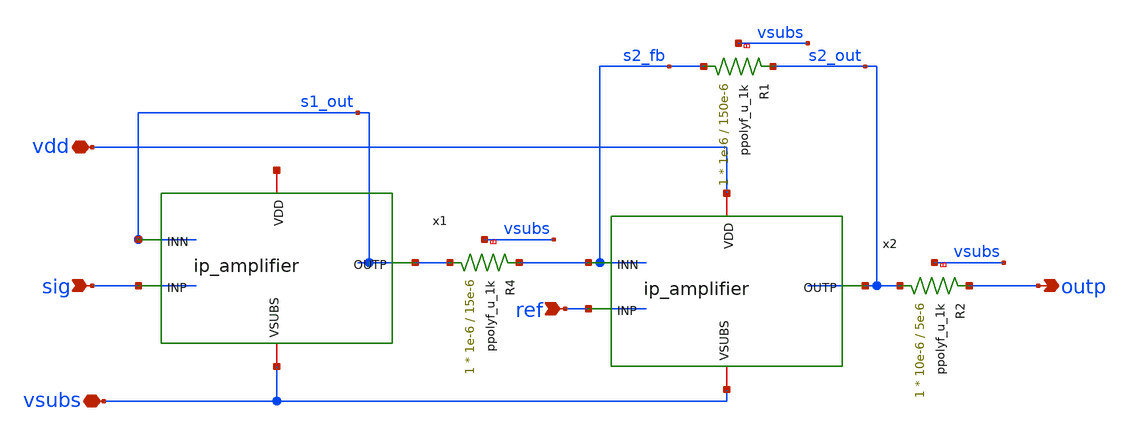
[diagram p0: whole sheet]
** sch_path: xschem/ip_sigproc.sch
**.subckt ip_sigproc sig ref vdd vsubs outp
*.ipin sig
*.ipin ref
*.iopin vdd
*.iopin vsubs
*.opin outp
x1 net1 s1_out sig s1_out vsubs ip_amplifier
x2 vdd s2_out ref s2_fb vsubs ip_amplifier
XR4 s1_out s2_fb vsubs ppolyf_u_1k r_width=1e-6 r_length=15e-6 m=1
XR1 s2_fb s2_out vsubs ppolyf_u_1k r_width=1e-6 r_length=150e-6 m=1
XR2 s2_out outp vsubs ppolyf_u_1k r_width=10e-6 r_length=5e-6 m=1
**.ends

* expanding   symbol:  ip_amplifier.sym # of pins=5
** sym_path: xschem/ip_amplifier.sym
** sch_path: xschem/ip_amplifier.sch
.subckt ip_amplifier VDD OUTP INP INN VSUBS
*.iopin VDD
*.iopin VSUBS
*.ipin INP
*.ipin INN
*.opin OUTP
XM1 net10 INP net8 VDD pfet_06v0 L=0.7u W=11.0u nf=1 ad='int((nf+1)/2) * W/nf * 0.18u' as='int((nf+2)/2) * W/nf * 0.18u'
+ pd='2*int((nf+1)/2) * (W/nf + 0.18u)' ps='2*int((nf+2)/2) * (W/nf + 0.18u)' nrd='0.18u / W' nrs='0.18u / W'
+ sa=0 sb=0 sd=0 m=2 par=2
XM2 net9 INN net8 VDD pfet_06v0 L=0.7u W=11.0u nf=1 ad='int((nf+1)/2) * W/nf * 0.18u' as='int((nf+2)/2) * W/nf * 0.18u'
+ pd='2*int((nf+1)/2) * (W/nf + 0.18u)' ps='2*int((nf+2)/2) * (W/nf + 0.18u)' nrd='0.18u / W' nrs='0.18u / W'
+ sa=0 sb=0 sd=0 m=2 par=2
XM5 net10 net1 VSUBS vsubs nfet_06v0 L=2u W=5u nf=1 ad='int((nf+1)/2) * W/nf * 0.18u' as='int((nf+2)/2) * W/nf * 0.18u'
+ pd='2*int((nf+1)/2) * (W/nf + 0.18u)' ps='2*int((nf+2)/2) * (W/nf + 0.18u)' nrd='0.18u / W' nrs='0.18u / W'
+ sa=0 sb=0 sd=0 m=1 par=1
XM6 net9 net1 VSUBS vsubs nfet_06v0 L=2u W=5u nf=1 ad='int((nf+1)/2) * W/nf * 0.18u' as='int((nf+2)/2) * W/nf * 0.18u'
+ pd='2*int((nf+1)/2) * (W/nf + 0.18u)' ps='2*int((nf+2)/2) * (W/nf + 0.18u)' nrd='0.18u / W' nrs='0.18u / W'
+ sa=0 sb=0 sd=0 m=1 par=1
XM3 net3 net1 VSUBS vsubs nfet_06v0 L=1u W=12.5u nf=1 ad='int((nf+1)/2) * W/nf * 0.18u' as='int((nf+2)/2) * W/nf * 0.18u'
+ pd='2*int((nf+1)/2) * (W/nf + 0.18u)' ps='2*int((nf+2)/2) * (W/nf + 0.18u)' nrd='0.18u / W' nrs='0.18u / W'
+ sa=0 sb=0 sd=0 m=2 par=2
XM4 net2 net1 VSUBS vsubs nfet_06v0 L=1u W=5u nf=1 ad='int((nf+1)/2) * W/nf * 0.18u' as='int((nf+2)/2) * W/nf * 0.18u'
+ pd='2*int((nf+1)/2) * (W/nf + 0.18u)' ps='2*int((nf+2)/2) * (W/nf + 0.18u)' nrd='0.18u / W' nrs='0.18u / W'
+ sa=0 sb=0 sd=0 m=1 par=1
XM7 net1 net1 net3 vsubs nfet_06v0 L=0.7u W=14u nf=1 ad='int((nf+1)/2) * W/nf * 0.18u' as='int((nf+2)/2) * W/nf * 0.18u'
+ pd='2*int((nf+1)/2) * (W/nf + 0.18u)' ps='2*int((nf+2)/2) * (W/nf + 0.18u)' nrd='0.18u / W' nrs='0.18u / W'
+ sa=0 sb=0 sd=0 m=2 par=2
XM8 net4 net1 net2 vsubs nfet_06v0 L=0.7u W=14u nf=1 ad='int((nf+1)/2) * W/nf * 0.18u' as='int((nf+2)/2) * W/nf * 0.18u'
+ pd='2*int((nf+1)/2) * (W/nf + 0.18u)' ps='2*int((nf+2)/2) * (W/nf + 0.18u)' nrd='0.18u / W' nrs='0.18u / W'
+ sa=0 sb=0 sd=0 m=2 par=2
XM9 net5 net7 VDD VDD pfet_06v0 L=1u W=6u nf=1 ad='int((nf+1)/2) * W/nf * 0.18u' as='int((nf+2)/2) * W/nf * 0.18u'
+ pd='2*int((nf+1)/2) * (W/nf + 0.18u)' ps='2*int((nf+2)/2) * (W/nf + 0.18u)' nrd='0.18u / W' nrs='0.18u / W'
+ sa=0 sb=0 sd=0 m=1 par=1
XM10 net6 net7 VDD VDD pfet_06v0 L=1u W=6u nf=1 ad='int((nf+1)/2) * W/nf * 0.18u' as='int((nf+2)/2) * W/nf * 0.18u'
+ pd='2*int((nf+1)/2) * (W/nf + 0.18u)' ps='2*int((nf+2)/2) * (W/nf + 0.18u)' nrd='0.18u / W' nrs='0.18u / W'
+ sa=0 sb=0 sd=0 m=1 par=1
XM11 net7 net7 net5 VDD pfet_06v0 L=0.7u W=14u nf=1 ad='int((nf+1)/2) * W/nf * 0.18u' as='int((nf+2)/2) * W/nf * 0.18u'
+ pd='2*int((nf+1)/2) * (W/nf + 0.18u)' ps='2*int((nf+2)/2) * (W/nf + 0.18u)' nrd='0.18u / W' nrs='0.18u / W'
+ sa=0 sb=0 sd=0 m=2 par=2
XM12 net8 net7 net6 VDD pfet_06v0 L=0.7u W=14u nf=1 ad='int((nf+1)/2) * W/nf * 0.18u' as='int((nf+2)/2) * W/nf * 0.18u'
+ pd='2*int((nf+1)/2) * (W/nf + 0.18u)' ps='2*int((nf+2)/2) * (W/nf + 0.18u)' nrd='0.18u / W' nrs='0.18u / W'
+ sa=0 sb=0 sd=0 m=2 par=2
XM13 net11 net1 net9 vsubs nfet_06v0 L=0.7u W=12u nf=1 ad='int((nf+1)/2) * W/nf * 0.18u' as='int((nf+2)/2) * W/nf * 0.18u'
+ pd='2*int((nf+1)/2) * (W/nf + 0.18u)' ps='2*int((nf+2)/2) * (W/nf + 0.18u)' nrd='0.18u / W' nrs='0.18u / W'
+ sa=0 sb=0 sd=0 m=1 par=1
XM14 COMP net1 net10 vsubs nfet_06v0 L=0.7u W=12u nf=1 ad='int((nf+1)/2) * W/nf * 0.18u' as='int((nf+2)/2) * W/nf * 0.18u'
+ pd='2*int((nf+1)/2) * (W/nf + 0.18u)' ps='2*int((nf+2)/2) * (W/nf + 0.18u)' nrd='0.18u / W' nrs='0.18u / W'
+ sa=0 sb=0 sd=0 m=1 par=1
XM15 net11 net11 VDD VDD pfet_06v0 L=0.7u W=12u nf=1 ad='int((nf+1)/2) * W/nf * 0.18u' as='int((nf+2)/2) * W/nf * 0.18u'
+ pd='2*int((nf+1)/2) * (W/nf + 0.18u)' ps='2*int((nf+2)/2) * (W/nf + 0.18u)' nrd='0.18u / W' nrs='0.18u / W'
+ sa=0 sb=0 sd=0 m=1 par=1
XM16 COMP net11 VDD VDD pfet_06v0 L=0.7u W=12u nf=1 ad='int((nf+1)/2) * W/nf * 0.18u' as='int((nf+2)/2) * W/nf * 0.18u'
+ pd='2*int((nf+1)/2) * (W/nf + 0.18u)' ps='2*int((nf+2)/2) * (W/nf + 0.18u)' nrd='0.18u / W' nrs='0.18u / W'
+ sa=0 sb=0 sd=0 m=1 par=1
XM17 OUTP COMP VDD VDD pfet_06v0 L=0.7u W=12u nf=1 ad='int((nf+1)/2) * W/nf * 0.18u' as='int((nf+2)/2) * W/nf * 0.18u'
+ pd='2*int((nf+1)/2) * (W/nf + 0.18u)' ps='2*int((nf+2)/2) * (W/nf + 0.18u)' nrd='0.18u / W' nrs='0.18u / W'
+ sa=0 sb=0 sd=0 m=5 par=5
XM18 OUTP net10 VSUBS vsubs nfet_06v0 L=0.7u W=12u nf=1 ad='int((nf+1)/2) * W/nf * 0.18u' as='int((nf+2)/2) * W/nf * 0.18u'
+ pd='2*int((nf+1)/2) * (W/nf + 0.18u)' ps='2*int((nf+2)/2) * (W/nf + 0.18u)' nrd='0.18u / W' nrs='0.18u / W'
+ sa=0 sb=0 sd=0 m=3 par=3
XR3 net1 net14 vsubs ppolyf_u_1k_6p0 r_width=1e-6 r_length=6e-6 m=1
XR6 net14 net13 vsubs ppolyf_u_1k_6p0 r_width=1e-6 r_length=6e-6 m=1
XR7 net13 net12 vsubs ppolyf_u_1k_6p0 r_width=1e-6 r_length=6e-6 m=1
XR8 net12 net15 vsubs ppolyf_u_1k_6p0 r_width=1e-6 r_length=4e-6 m=1
Vmeas VDD net15 0
Vmeas1 net7 net4 0
XC1 OUTP net16 cap_nmos_03v3 c_width=12e-6 c_length=18e-6 m=1
XC2 COMP net17 cap_nmos_03v3 c_width=12e-6 c_length=18e-6 m=1
XR12 net16 COMP vsubs ppolyf_u_1k_6p0 r_width=1e-6 r_length=10e-6 m=1
XR16 OUTP net17 vsubs ppolyf_u_1k_6p0 r_width=1e-6 r_length=10e-6 m=1
.ends

.end
